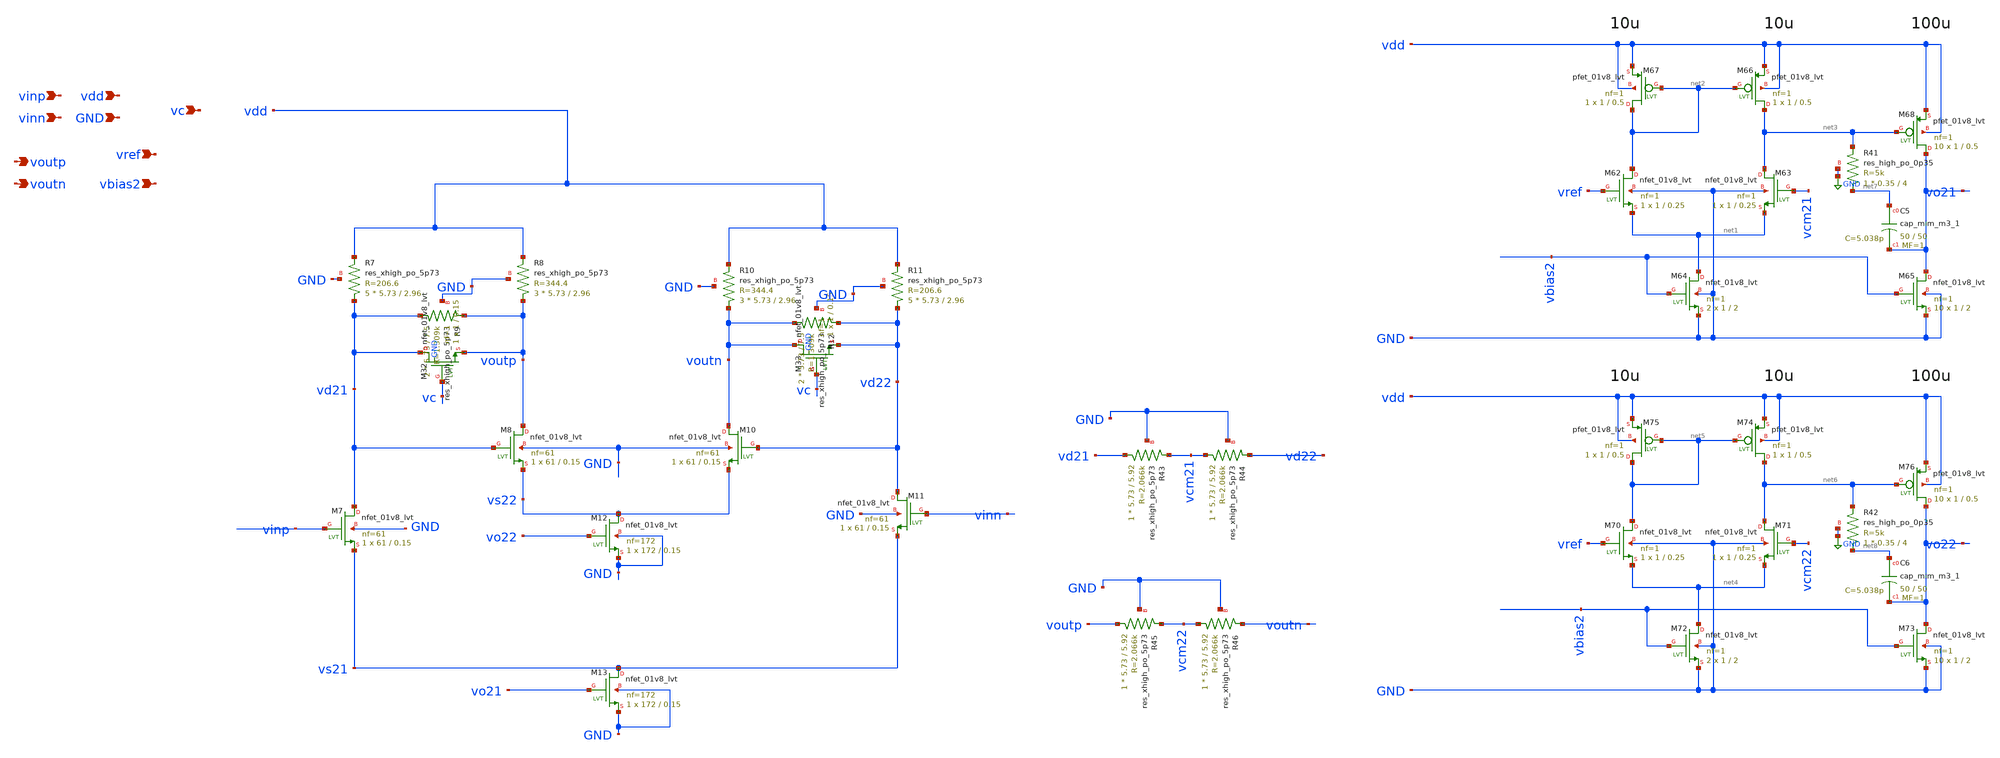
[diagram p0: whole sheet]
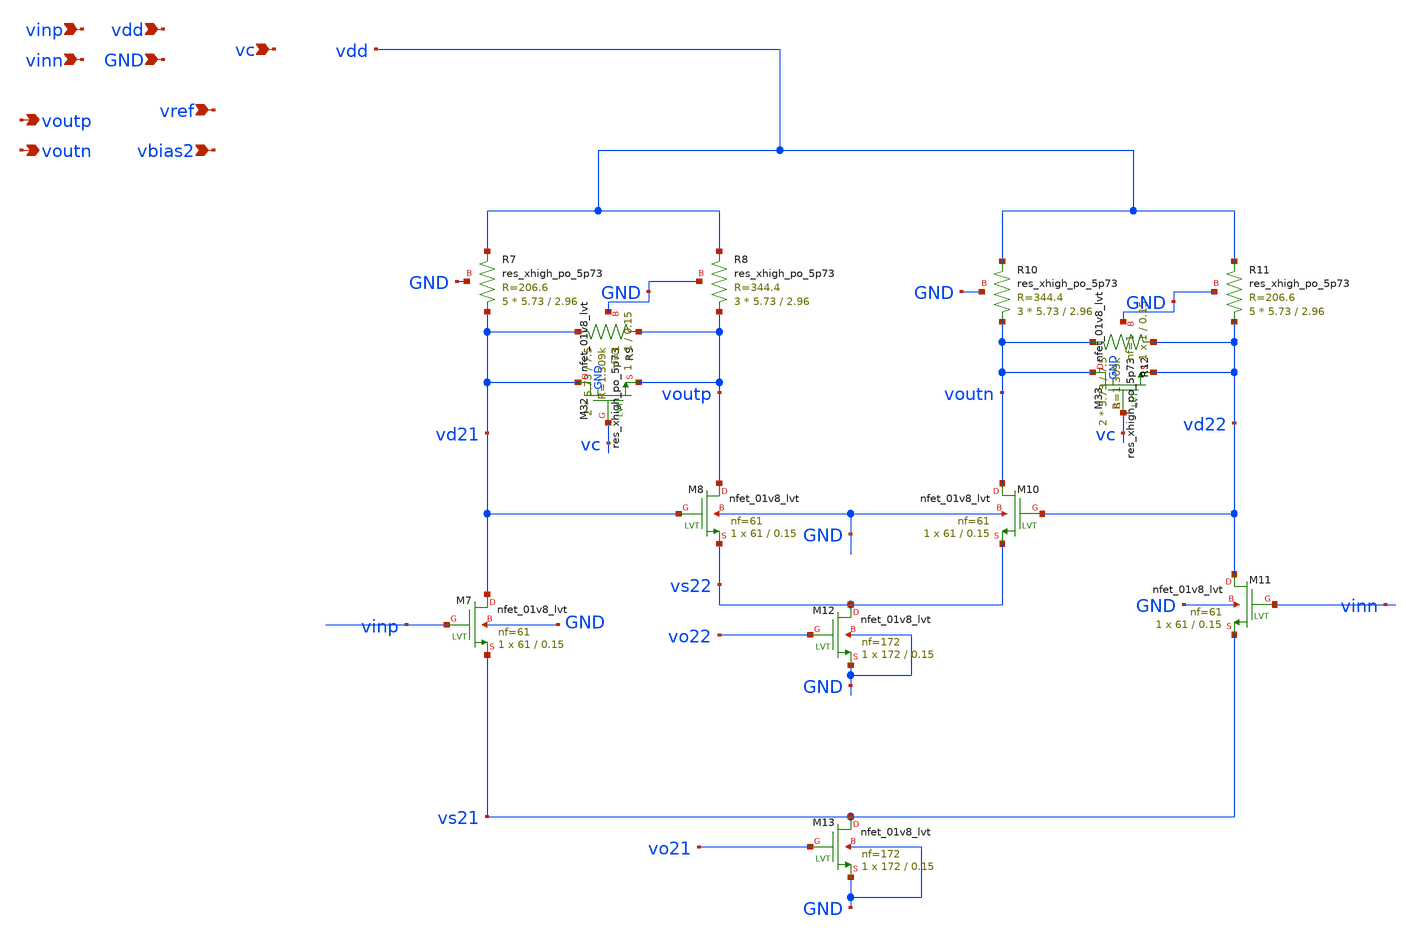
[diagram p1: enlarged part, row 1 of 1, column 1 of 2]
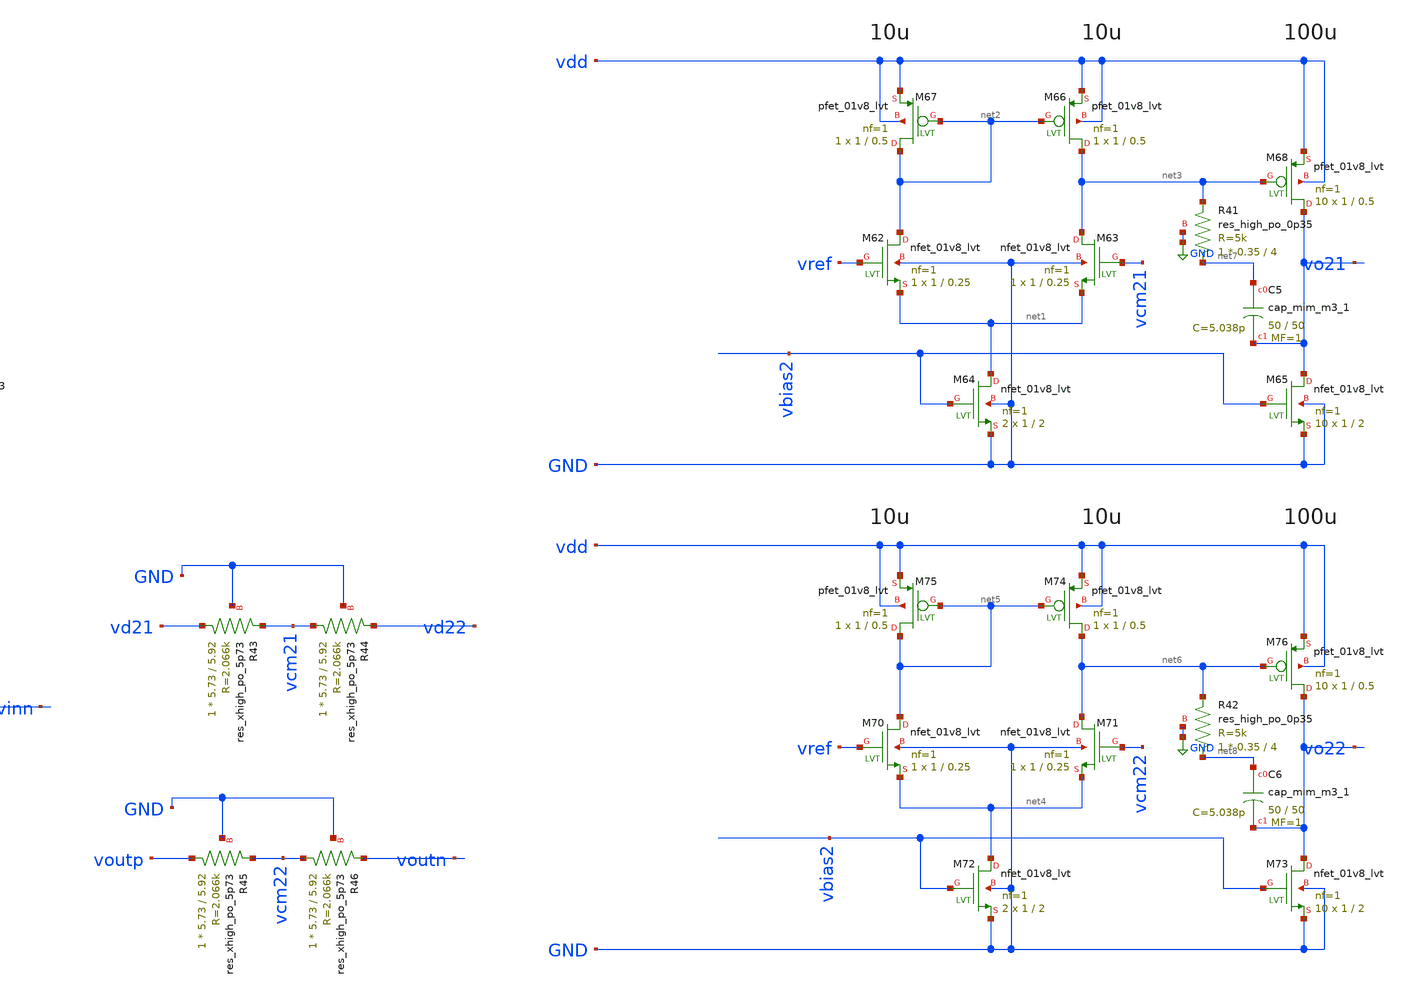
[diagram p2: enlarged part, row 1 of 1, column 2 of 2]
** sch_path: xschem/vga/VGA_unit.sch
**.subckt VGA_unit vinp vinn voutp voutn vdd GND vref vbias2 vc
*.ipin vinp
*.ipin vinn
*.opin voutp
*.opin voutn
*.ipin vdd
*.ipin GND
*.ipin vref
*.ipin vbias2
*.ipin vc
XR7 vd21 vdd GND sky130_fd_pr__res_xhigh_po_5p73 L=2.96 mult=5 m=5
XR8 voutp vdd GND sky130_fd_pr__res_xhigh_po_5p73 L=2.96 mult=3 m=3
XR9 vd21 voutp GND sky130_fd_pr__res_xhigh_po_5p73 L=7.5 mult=2 m=2
XR10 voutn vdd GND sky130_fd_pr__res_xhigh_po_5p73 L=2.96 mult=3 m=3
XR11 vd22 vdd GND sky130_fd_pr__res_xhigh_po_5p73 L=2.96 mult=5 m=5
XR12 voutn vd22 GND sky130_fd_pr__res_xhigh_po_5p73 L=7.5 mult=2 m=2
XM7 vd21 vinp vs21 GND sky130_fd_pr__nfet_01v8_lvt L=0.15 W=61 nf=61 ad='int((nf+1)/2) * W/nf * 0.29'
+ as='int((nf+2)/2) * W/nf * 0.29' pd='2*int((nf+1)/2) * (W/nf + 0.29)' ps='2*int((nf+2)/2) * (W/nf + 0.29)'
+ nrd='0.29 / W' nrs='0.29 / W' sa=0 sb=0 sd=0 mult=1 m=1
XM8 voutp vd21 vs22 GND sky130_fd_pr__nfet_01v8_lvt L=0.15 W=61 nf=61 ad='int((nf+1)/2) * W/nf * 0.29'
+ as='int((nf+2)/2) * W/nf * 0.29' pd='2*int((nf+1)/2) * (W/nf + 0.29)' ps='2*int((nf+2)/2) * (W/nf + 0.29)'
+ nrd='0.29 / W' nrs='0.29 / W' sa=0 sb=0 sd=0 mult=1 m=1
XM10 voutn vd22 vs22 GND sky130_fd_pr__nfet_01v8_lvt L=0.15 W=61 nf=61 ad='int((nf+1)/2) * W/nf * 0.29'
+ as='int((nf+2)/2) * W/nf * 0.29' pd='2*int((nf+1)/2) * (W/nf + 0.29)' ps='2*int((nf+2)/2) * (W/nf + 0.29)'
+ nrd='0.29 / W' nrs='0.29 / W' sa=0 sb=0 sd=0 mult=1 m=1
XM11 vd22 vinn vs21 GND sky130_fd_pr__nfet_01v8_lvt L=0.15 W=61 nf=61 ad='int((nf+1)/2) * W/nf * 0.29'
+ as='int((nf+2)/2) * W/nf * 0.29' pd='2*int((nf+1)/2) * (W/nf + 0.29)' ps='2*int((nf+2)/2) * (W/nf + 0.29)'
+ nrd='0.29 / W' nrs='0.29 / W' sa=0 sb=0 sd=0 mult=1 m=1
XM12 vs22 vo22 GND GND sky130_fd_pr__nfet_01v8_lvt L=0.15 W=172 nf=172 ad='int((nf+1)/2) * W/nf * 0.29'
+ as='int((nf+2)/2) * W/nf * 0.29' pd='2*int((nf+1)/2) * (W/nf + 0.29)' ps='2*int((nf+2)/2) * (W/nf + 0.29)'
+ nrd='0.29 / W' nrs='0.29 / W' sa=0 sb=0 sd=0 mult=1 m=1
XM13 vs21 vo21 GND GND sky130_fd_pr__nfet_01v8_lvt L=0.15 W=172 nf=172 ad='int((nf+1)/2) * W/nf * 0.29'
+ as='int((nf+2)/2) * W/nf * 0.29' pd='2*int((nf+1)/2) * (W/nf + 0.29)' ps='2*int((nf+2)/2) * (W/nf + 0.29)'
+ nrd='0.29 / W' nrs='0.29 / W' sa=0 sb=0 sd=0 mult=1 m=1
XM32 vd21 vc voutp GND sky130_fd_pr__nfet_01v8_lvt L=0.15 W=1 nf=1 ad='int((nf+1)/2) * W/nf * 0.29' as='int((nf+2)/2) * W/nf * 0.29'
+ pd='2*int((nf+1)/2) * (W/nf + 0.29)' ps='2*int((nf+2)/2) * (W/nf + 0.29)' nrd='0.29 / W' nrs='0.29 / W'
+ sa=0 sb=0 sd=0 mult=1 m=1
XM33 voutn vc vd22 GND sky130_fd_pr__nfet_01v8_lvt L=0.15 W=1 nf=1 ad='int((nf+1)/2) * W/nf * 0.29' as='int((nf+2)/2) * W/nf * 0.29'
+ pd='2*int((nf+1)/2) * (W/nf + 0.29)' ps='2*int((nf+2)/2) * (W/nf + 0.29)' nrd='0.29 / W' nrs='0.29 / W'
+ sa=0 sb=0 sd=0 mult=1 m=1
XM62 net2 vref net1 GND sky130_fd_pr__nfet_01v8_lvt L=0.25 W=1 nf=1 ad='int((nf+1)/2) * W/nf * 0.29'
+ as='int((nf+2)/2) * W/nf * 0.29' pd='2*int((nf+1)/2) * (W/nf + 0.29)' ps='2*int((nf+2)/2) * (W/nf + 0.29)'
+ nrd='0.29 / W' nrs='0.29 / W' sa=0 sb=0 sd=0 mult=1 m=1
XM63 net3 vcm21 net1 GND sky130_fd_pr__nfet_01v8_lvt L=0.25 W=1 nf=1 ad='int((nf+1)/2) * W/nf * 0.29'
+ as='int((nf+2)/2) * W/nf * 0.29' pd='2*int((nf+1)/2) * (W/nf + 0.29)' ps='2*int((nf+2)/2) * (W/nf + 0.29)'
+ nrd='0.29 / W' nrs='0.29 / W' sa=0 sb=0 sd=0 mult=1 m=1
XM64 net1 vbias2 GND GND sky130_fd_pr__nfet_01v8_lvt L=2 W=1 nf=1 ad='int((nf+1)/2) * W/nf * 0.29' as='int((nf+2)/2) * W/nf * 0.29'
+ pd='2*int((nf+1)/2) * (W/nf + 0.29)' ps='2*int((nf+2)/2) * (W/nf + 0.29)' nrd='0.29 / W' nrs='0.29 / W'
+ sa=0 sb=0 sd=0 mult=2 m=2
XM65 vo21 vbias2 GND GND sky130_fd_pr__nfet_01v8_lvt L=2 W=1 nf=1 ad='int((nf+1)/2) * W/nf * 0.29' as='int((nf+2)/2) * W/nf * 0.29'
+ pd='2*int((nf+1)/2) * (W/nf + 0.29)' ps='2*int((nf+2)/2) * (W/nf + 0.29)' nrd='0.29 / W' nrs='0.29 / W'
+ sa=0 sb=0 sd=0 mult=10 m=10
XM66 net3 net2 vdd vdd sky130_fd_pr__pfet_01v8_lvt L=0.5 W=1 nf=1 ad='int((nf+1)/2) * W/nf * 0.29' as='int((nf+2)/2) * W/nf * 0.29'
+ pd='2*int((nf+1)/2) * (W/nf + 0.29)' ps='2*int((nf+2)/2) * (W/nf + 0.29)' nrd='0.29 / W' nrs='0.29 / W'
+ sa=0 sb=0 sd=0 mult=1 m=1
XM67 net2 net2 vdd vdd sky130_fd_pr__pfet_01v8_lvt L=0.5 W=1 nf=1 ad='int((nf+1)/2) * W/nf * 0.29' as='int((nf+2)/2) * W/nf * 0.29'
+ pd='2*int((nf+1)/2) * (W/nf + 0.29)' ps='2*int((nf+2)/2) * (W/nf + 0.29)' nrd='0.29 / W' nrs='0.29 / W'
+ sa=0 sb=0 sd=0 mult=1 m=1
XM68 vo21 net3 vdd vdd sky130_fd_pr__pfet_01v8_lvt L=0.5 W=1 nf=1 ad='int((nf+1)/2) * W/nf * 0.29' as='int((nf+2)/2) * W/nf * 0.29'
+ pd='2*int((nf+1)/2) * (W/nf + 0.29)' ps='2*int((nf+2)/2) * (W/nf + 0.29)' nrd='0.29 / W' nrs='0.29 / W'
+ sa=0 sb=0 sd=0 mult=10 m=10
XC5 net7 vo21 sky130_fd_pr__cap_mim_m3_1 W=50 L=50 MF=1 m=1
XM70 net5 vref net4 GND sky130_fd_pr__nfet_01v8_lvt L=0.25 W=1 nf=1 ad='int((nf+1)/2) * W/nf * 0.29'
+ as='int((nf+2)/2) * W/nf * 0.29' pd='2*int((nf+1)/2) * (W/nf + 0.29)' ps='2*int((nf+2)/2) * (W/nf + 0.29)'
+ nrd='0.29 / W' nrs='0.29 / W' sa=0 sb=0 sd=0 mult=1 m=1
XM71 net6 vcm22 net4 GND sky130_fd_pr__nfet_01v8_lvt L=0.25 W=1 nf=1 ad='int((nf+1)/2) * W/nf * 0.29'
+ as='int((nf+2)/2) * W/nf * 0.29' pd='2*int((nf+1)/2) * (W/nf + 0.29)' ps='2*int((nf+2)/2) * (W/nf + 0.29)'
+ nrd='0.29 / W' nrs='0.29 / W' sa=0 sb=0 sd=0 mult=1 m=1
XM72 net4 vbias2 GND GND sky130_fd_pr__nfet_01v8_lvt L=2 W=1 nf=1 ad='int((nf+1)/2) * W/nf * 0.29' as='int((nf+2)/2) * W/nf * 0.29'
+ pd='2*int((nf+1)/2) * (W/nf + 0.29)' ps='2*int((nf+2)/2) * (W/nf + 0.29)' nrd='0.29 / W' nrs='0.29 / W'
+ sa=0 sb=0 sd=0 mult=2 m=2
XM73 vo22 vbias2 GND GND sky130_fd_pr__nfet_01v8_lvt L=2 W=1 nf=1 ad='int((nf+1)/2) * W/nf * 0.29' as='int((nf+2)/2) * W/nf * 0.29'
+ pd='2*int((nf+1)/2) * (W/nf + 0.29)' ps='2*int((nf+2)/2) * (W/nf + 0.29)' nrd='0.29 / W' nrs='0.29 / W'
+ sa=0 sb=0 sd=0 mult=10 m=10
XM74 net6 net5 vdd vdd sky130_fd_pr__pfet_01v8_lvt L=0.5 W=1 nf=1 ad='int((nf+1)/2) * W/nf * 0.29' as='int((nf+2)/2) * W/nf * 0.29'
+ pd='2*int((nf+1)/2) * (W/nf + 0.29)' ps='2*int((nf+2)/2) * (W/nf + 0.29)' nrd='0.29 / W' nrs='0.29 / W'
+ sa=0 sb=0 sd=0 mult=1 m=1
XM75 net5 net5 vdd vdd sky130_fd_pr__pfet_01v8_lvt L=0.5 W=1 nf=1 ad='int((nf+1)/2) * W/nf * 0.29' as='int((nf+2)/2) * W/nf * 0.29'
+ pd='2*int((nf+1)/2) * (W/nf + 0.29)' ps='2*int((nf+2)/2) * (W/nf + 0.29)' nrd='0.29 / W' nrs='0.29 / W'
+ sa=0 sb=0 sd=0 mult=1 m=1
XM76 vo22 net6 vdd vdd sky130_fd_pr__pfet_01v8_lvt L=0.5 W=1 nf=1 ad='int((nf+1)/2) * W/nf * 0.29' as='int((nf+2)/2) * W/nf * 0.29'
+ pd='2*int((nf+1)/2) * (W/nf + 0.29)' ps='2*int((nf+2)/2) * (W/nf + 0.29)' nrd='0.29 / W' nrs='0.29 / W'
+ sa=0 sb=0 sd=0 mult=10 m=10
XC6 net8 vo22 sky130_fd_pr__cap_mim_m3_1 W=50 L=50 MF=1 m=1
XR43 vd21 vcm21 GND sky130_fd_pr__res_xhigh_po_5p73 L=5.92 mult=1 m=1
XR44 vcm21 vd22 GND sky130_fd_pr__res_xhigh_po_5p73 L=5.92 mult=1 m=1
XR45 voutp vcm22 GND sky130_fd_pr__res_xhigh_po_5p73 L=5.92 mult=1 m=1
XR46 vcm22 voutn GND sky130_fd_pr__res_xhigh_po_5p73 L=5.92 mult=1 m=1
XR41 net7 net3 GND sky130_fd_pr__res_high_po_0p35 L=4 mult=1 m=1
XR42 net8 net6 GND sky130_fd_pr__res_high_po_0p35 L=4 mult=1 m=1
**.ends
.GLOBAL GND
.end
